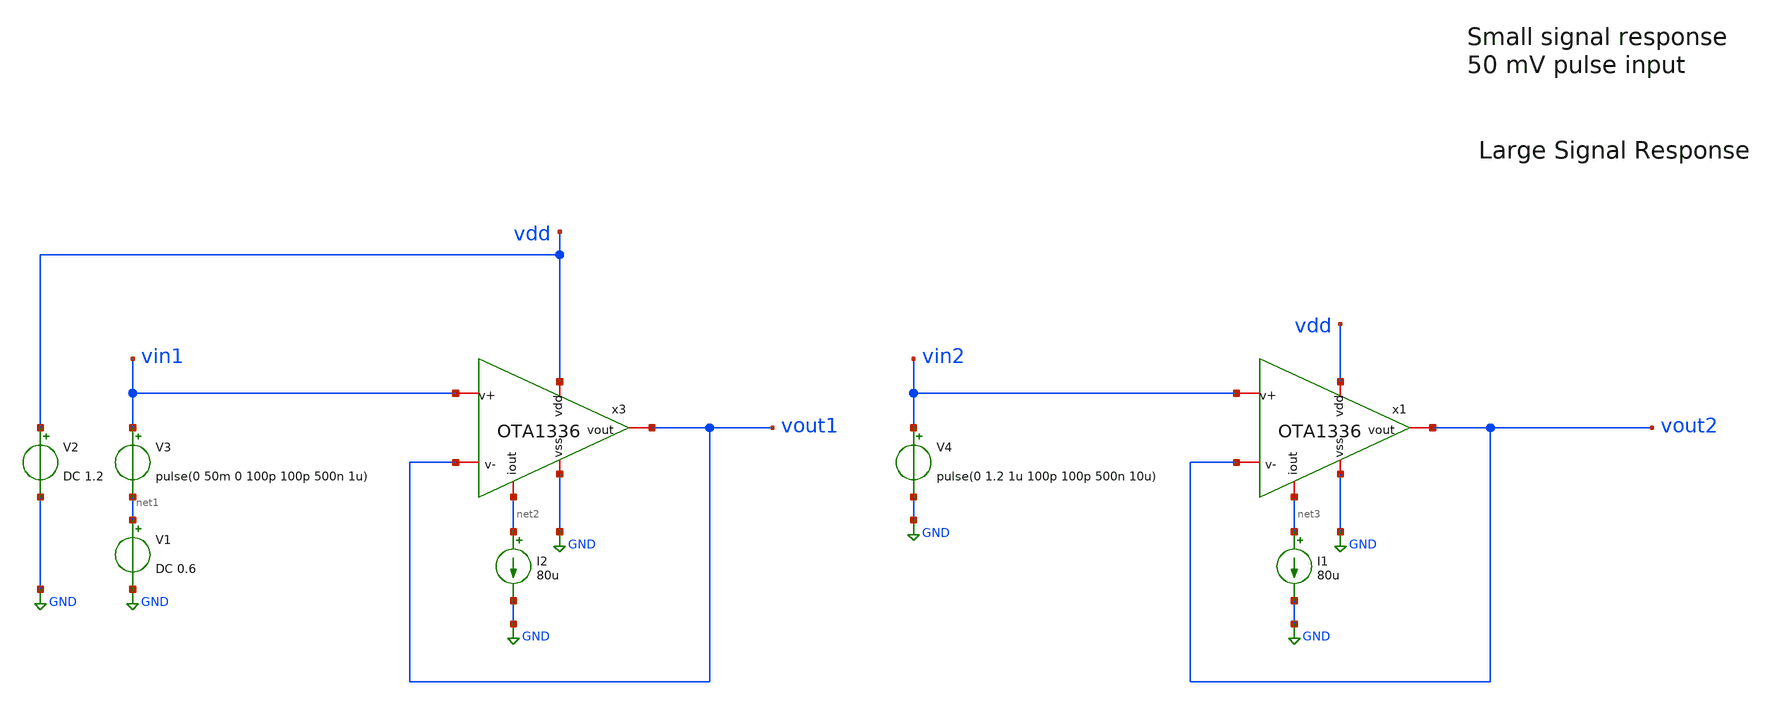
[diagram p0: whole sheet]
** sch_path: tests/data/OTA1336/testbenches/tran/xschem/OTA1336_overshoot_tb.sch
**.subckt OTA1336_overshoot_tb
I2 net2 GND 80u
V2 vdd GND DC 1.2
x3 vdd net2 vout1 vout1 vin1 GND OTA1336
V3 vin1 net1 pulse(0 50m 0 100p 100p 500n 1u)
V1 net1 GND DC 0.6
I1 net3 GND 80u
x1 vdd net3 vout2 vout2 vin2 GND OTA1336
V4 vin2 GND pulse(0 1.2 1u 100p 100p 500n 10u)
**** begin user architecture code

.lib cornerCAP.lib cap_typ
.lib cornerMOSlv.lib mos_tt
.lib cornerRES.lib res_typ



.control
save all
tran 1n 5u
meas tran Vmax MAX v(vout1) from=750n to=1.5u
let ovshoot = $&vmax/0.65
echo $&ovshoot
write slew_rate.raw

.endc


**** end user architecture code
**.ends
.GLOBAL GND
.end
